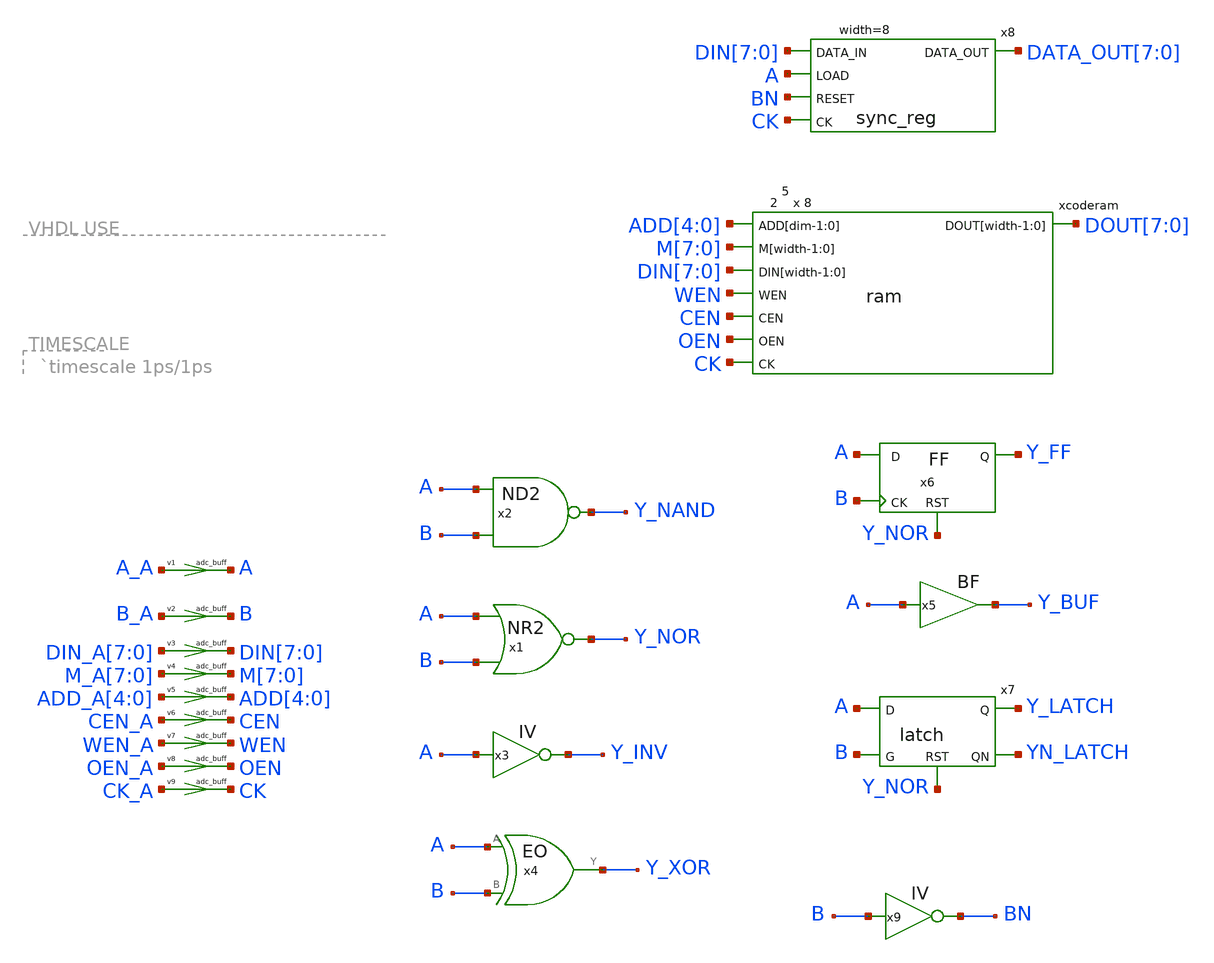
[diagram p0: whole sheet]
** sch_path: xschem_library/logic/testbench.sch
**.subckt testbench
x1 [ A B ] Y_NOR nor
x2 [ A B ] Y_NAND nand
x3 [ A ] Y_INV inv
x4 Y_XOR A B eo
x5 Y_BUF A bf
x6 A Y_FF B Y_NOR ff
x7 A Y_LATCH B Y_NOR YN_LATCH latch
xcoderam ADD[4] ADD[3] ADD[2] ADD[1] ADD[0] M[7] M[6] M[5] M[4] M[3] M[2] M[1] M[0] DOUT[7] DOUT[6]
+ DOUT[5] DOUT[4] DOUT[3] DOUT[2] DOUT[1] DOUT[0] DIN[7] DIN[6] DIN[5] DIN[4] DIN[3] DIN[2] DIN[1] DIN[0] WEN
+ CEN OEN CK ram
x8 DATA_OUT[7] DATA_OUT[6] DATA_OUT[5] DATA_OUT[4] DATA_OUT[3] DATA_OUT[2] DATA_OUT[1] DATA_OUT[0]
+ CK BN DIN[7] DIN[6] DIN[5] DIN[4] DIN[3] DIN[2] DIN[1] DIN[0] A sync_reg
x9 [ B ] BN inv
v1 [ A_A ] [ A ] adc_buff
v2 [ B_A ] [ B ] adc_buff
v3 [ DIN_A[7] ] [ DIN[7] ] adc_buff
v4 [ M_A[7] ] [ M[7] ] adc_buff
v5 [ ADD_A[4] ] [ ADD[4] ] adc_buff
v6 [ CEN_A ] [ CEN ] adc_buff
v7 [ WEN_A ] [ WEN ] adc_buff
v8 [ OEN_A ] [ OEN ] adc_buff
v9 [ CK_A ] [ CK ] adc_buff
**.ends

* expanding   symbol:  eo.sym # of pins=3
** sym_path: xschem_library/logic/eo.sym
** sch_path: xschem_library/logic/eo.sch
.subckt eo Y A B  delay=220 ps del=220
*.ipin A
*.ipin B
*.opin Y
.ends


* expanding   symbol:  bf.sym # of pins=2
** sym_path: xschem_library/logic/bf.sym
** sch_path: xschem_library/logic/bf.sch
.subckt bf Y A  delay=90 ps del=90
*.opin Y
*.ipin A
.ends


* expanding   symbol:  ff.sym # of pins=4
** sym_path: xschem_library/logic/ff.sym
** sch_path: xschem_library/logic/ff.sch
.subckt ff D Q CK RST  delay=400 ps del=400
*.ipin D
*.opin Q
*.ipin CK
*.ipin RST
.ends


* expanding   symbol:  latch.sym # of pins=5
** sym_path: xschem_library/logic/latch.sym
** sch_path: xschem_library/logic/latch.sch
.subckt latch D Q G RST QN  delay=200 ps del=200
*.opin Q
*.ipin G
*.ipin RST
*.opin QN
*.ipin D
.ends


* expanding   symbol:  ram.sym # of pins=8
** sym_path: xschem_library/logic/ram.sym
** sch_path: xschem_library/logic/ram.sch
.subckt ram ADD[dim-1:0] M[width-1:0] DOUT[width-1:0] DIN[width-1:0] WEN CEN OEN CK  dim=5 width=8
+ hex=0
datafile=ram.list modulename=ram access_delay=3000 oe_delay=300
*.opin DOUT[width-1:0]
*.ipin DIN[width-1:0]
*.ipin CK
*.ipin OEN
*.ipin ADD[dim-1:0]
*.ipin WEN
*.ipin CEN
*.ipin M[width-1:0]
.ends


* expanding   symbol:  sync_reg.sym # of pins=5
** sym_path: xschem_library/logic/sync_reg.sym
** sch_path: xschem_library/logic/sync_reg.sch
.subckt sync_reg DATA_OUT[width-1:0] CK RESET DATA_IN[width-1:0] LOAD  width=8 del=400 delay=400 ps
*.opin DATA_OUT[width-1:0]
*.ipin CK
*.ipin RESET
*.ipin DATA_IN[width-1:0]
*.ipin LOAD
.ends

.end
